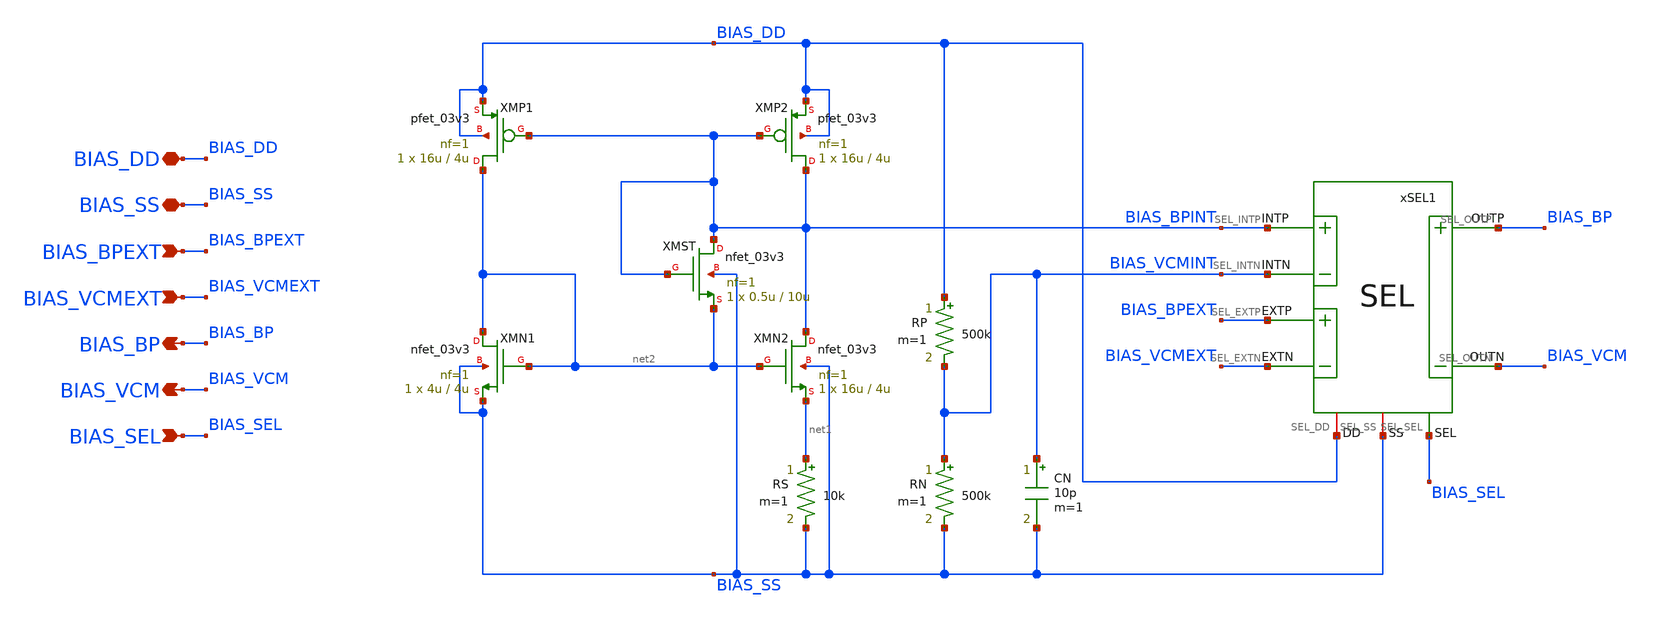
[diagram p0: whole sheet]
** sch_path: Design_Files/IC Design/Schematic/BIAS/BIAS.sch
**.subckt BIAS BIAS_DD BIAS_SS BIAS_BPEXT BIAS_VCMEXT BIAS_BP BIAS_VCM BIAS_SEL
*.iopin BIAS_DD
*.iopin BIAS_SS
*.ipin BIAS_BPEXT
*.ipin BIAS_VCMEXT
*.opin BIAS_BP
*.opin BIAS_VCM
*.ipin BIAS_SEL
XMN2 BIAS_BPINT net2 net1 BIAS_SS nfet_03v3 L=4u W=16u nf=1 ad='int((nf+1)/2) * W/nf * 0.18u' as='int((nf+2)/2) * W/nf * 0.18u'
+ pd='2*int((nf+1)/2) * (W/nf + 0.18u)' ps='2*int((nf+2)/2) * (W/nf + 0.18u)' nrd='0.18u / W' nrs='0.18u / W'
+ sa=0 sb=0 sd=0 m=1
XMP2 BIAS_BPINT BIAS_BPINT BIAS_DD BIAS_DD pfet_03v3 L=4u W=16u nf=1 ad='int((nf+1)/2) * W/nf * 0.18u'
+ as='int((nf+2)/2) * W/nf * 0.18u' pd='2*int((nf+1)/2) * (W/nf + 0.18u)' ps='2*int((nf+2)/2) * (W/nf + 0.18u)'
+ nrd='0.18u / W' nrs='0.18u / W' sa=0 sb=0 sd=0 m=1
XMN1 net2 net2 BIAS_SS BIAS_SS nfet_03v3 L=4u W=4u nf=1 ad='int((nf+1)/2) * W/nf * 0.18u' as='int((nf+2)/2) * W/nf * 0.18u'
+ pd='2*int((nf+1)/2) * (W/nf + 0.18u)' ps='2*int((nf+2)/2) * (W/nf + 0.18u)' nrd='0.18u / W' nrs='0.18u / W'
+ sa=0 sb=0 sd=0 m=1
XMP1 net2 BIAS_BPINT BIAS_DD BIAS_DD pfet_03v3 L=4u W=16u nf=1 ad='int((nf+1)/2) * W/nf * 0.18u' as='int((nf+2)/2) * W/nf * 0.18u'
+ pd='2*int((nf+1)/2) * (W/nf + 0.18u)' ps='2*int((nf+2)/2) * (W/nf + 0.18u)' nrd='0.18u / W' nrs='0.18u / W'
+ sa=0 sb=0 sd=0 m=1
RS net1 BIAS_SS 10k m=1
XMST BIAS_BPINT BIAS_BPINT net2 BIAS_SS nfet_03v3 L=10u W=0.5u nf=1 ad='int((nf+1)/2) * W/nf * 0.18u'
+ as='int((nf+2)/2) * W/nf * 0.18u' pd='2*int((nf+1)/2) * (W/nf + 0.18u)' ps='2*int((nf+2)/2) * (W/nf + 0.18u)'
+ nrd='0.18u / W' nrs='0.18u / W' sa=0 sb=0 sd=0 m=1
RP BIAS_DD BIAS_VCMINT 500k m=1
RN BIAS_VCMINT BIAS_SS 500k m=1
xSEL1 BIAS_DD BIAS_SS BIAS_BPINT BIAS_VCMINT BIAS_VCM BIAS_BP BIAS_BPEXT BIAS_VCMEXT BIAS_SEL SEL
CN BIAS_VCMINT BIAS_SS 10p m=1
**.ends

* expanding   symbol:  ECG_Acquisition_IC/Design_Files/IC Design/Schematic/SEL/SEL.sym # of pins=9
** sym_path: Design_Files/IC Design/Schematic/SEL/SEL.sym
** sch_path: Design_Files/IC Design/Schematic/SEL/SEL.sch
.subckt SEL SEL_DD SEL_SS SEL_INTP SEL_INTN SEL_OUTN SEL_OUTP SEL_EXTP SEL_EXTN SEL_SEL
*.iopin SEL_DD
*.iopin SEL_SS
*.ipin SEL_INTP
*.ipin SEL_INTN
*.iopin SEL_OUTP
*.iopin SEL_OUTN
*.ipin SEL_EXTP
*.ipin SEL_EXTN
*.ipin SEL_SEL
xINV1 SEL_DD SEL_SS SEL_SEL SELB INV
xTG1 SEL_DD SEL_SS SEL_EXTP SEL_OUTP SEL_SEL SELB TG
xTG2 SEL_DD SEL_SS SEL_INTP SEL_OUTP SELB SEL_SEL TG
xTG3 SEL_DD SEL_SS SEL_EXTN SEL_OUTN SEL_SEL SELB TG
xTG4 SEL_DD SEL_SS SEL_INTN SEL_OUTN SELB SEL_SEL TG
.ends


* expanding   symbol:  ECG_Acquisition_IC/Design_Files/IC Design/Schematic/INV/INV.sym # of pins=4
** sym_path: Design_Files/IC Design/Schematic/INV/INV.sym
** sch_path: Design_Files/IC Design/Schematic/INV/INV.sch
.subckt INV INV_DD INV_SS INV_IN INV_OUT
*.iopin INV_DD
*.iopin INV_SS
*.ipin INV_IN
*.opin INV_OUT
XMINVP INV_OUT INV_IN INV_DD INV_DD pfet_03v3 L=0.5u W=2u nf=1 ad='int((nf+1)/2) * W/nf * 0.18u' as='int((nf+2)/2) * W/nf * 0.18u'
+ pd='2*int((nf+1)/2) * (W/nf + 0.18u)' ps='2*int((nf+2)/2) * (W/nf + 0.18u)' nrd='0.18u / W' nrs='0.18u / W'
+ sa=0 sb=0 sd=0 m=1
XMINVN INV_OUT INV_IN INV_SS INV_SS nfet_03v3 L=0.5u W=1u nf=1 ad='int((nf+1)/2) * W/nf * 0.18u' as='int((nf+2)/2) * W/nf * 0.18u'
+ pd='2*int((nf+1)/2) * (W/nf + 0.18u)' ps='2*int((nf+2)/2) * (W/nf + 0.18u)' nrd='0.18u / W' nrs='0.18u / W'
+ sa=0 sb=0 sd=0 m=1
.ends


* expanding   symbol:  ECG_Acquisition_IC/Design_Files/IC Design/Schematic/TG/TG.sym # of pins=6
** sym_path: Design_Files/IC Design/Schematic/TG/TG.sym
** sch_path: Design_Files/IC Design/Schematic/TG/TG.sch
.subckt TG TG_DD TG_SS TG_A TG_B TG_SEL TG_SELB
*.iopin TG_DD
*.iopin TG_SS
*.iopin TG_A
*.iopin TG_B
*.ipin TG_SEL
*.ipin TG_SELB
XMTGP TG_B TG_SELB TG_A TG_DD pfet_03v3 L=0.5u W=40u nf=1 ad='int((nf+1)/2) * W/nf * 0.18u' as='int((nf+2)/2) * W/nf * 0.18u'
+ pd='2*int((nf+1)/2) * (W/nf + 0.18u)' ps='2*int((nf+2)/2) * (W/nf + 0.18u)' nrd='0.18u / W' nrs='0.18u / W'
+ sa=0 sb=0 sd=0 m=1
XMTGN TG_A TG_SEL TG_B TG_SS nfet_03v3 L=0.5u W=20u nf=1 ad='int((nf+1)/2) * W/nf * 0.18u' as='int((nf+2)/2) * W/nf * 0.18u'
+ pd='2*int((nf+1)/2) * (W/nf + 0.18u)' ps='2*int((nf+2)/2) * (W/nf + 0.18u)' nrd='0.18u / W' nrs='0.18u / W'
+ sa=0 sb=0 sd=0 m=1
.ends

.end
